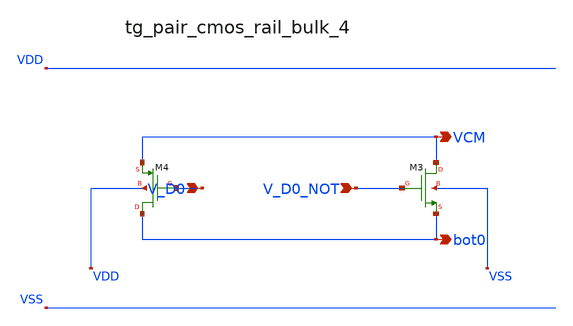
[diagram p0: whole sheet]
** sch_path: analog-db/raw/sw_003_binary_capbank/hier/blocks/tg_pair_cmos_rail_bulk_4.sch
**.subckt tg_pair_cmos_rail_bulk_4 V_D0 V_D0_NOT VCM bot0
*.ipin V_D0
*.ipin V_D0_NOT
*.opin VCM
*.opin bot0
XM3 VCM V_D0_NOT bot0 VSS sg13_lv_nmos w=x_dut_xm3_w l=x_dut_xm3_l ng=1 m=x_dut_xm3_m
XM4 bot0 V_D0 VCM VDD sg13_lv_pmos w=x_dut_xm4_w l=x_dut_xm4_l ng=1 m=x_dut_xm4_m
**.ends
.end
